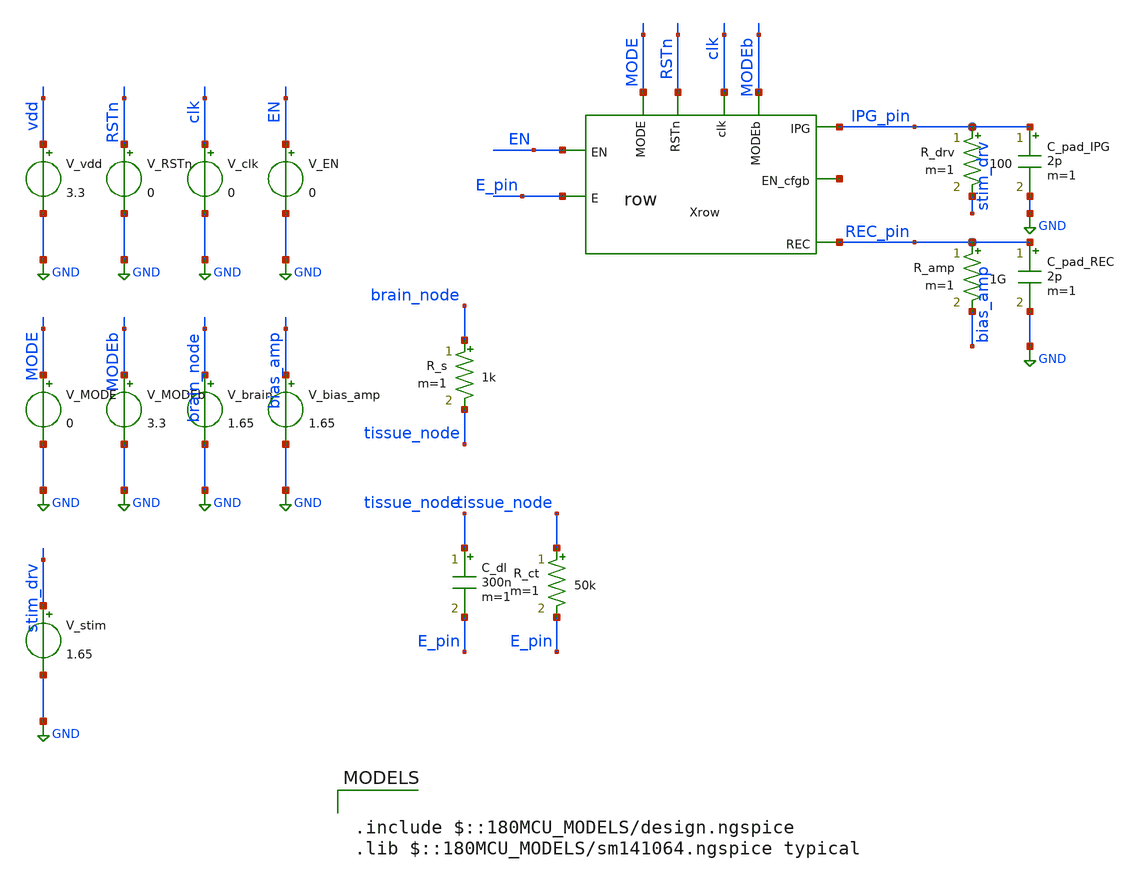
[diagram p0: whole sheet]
** sch_path: tb_realistic.sch
**.subckt tb_realistic
V_vdd vdd GND 3.3
V_RSTn RSTn GND 0
V_clk clk GND 0
V_EN EN GND 0
V_MODE MODE GND 0
V_MODEb MODEb GND 3.3
V_brain brain_node GND 1.65
V_bias_amp bias_amp GND 1.65
V_stim stim_drv GND 1.65
Xrow IPG_pin MODEb EN net1 clk E_pin MODE RSTn REC_pin row
R_s brain_node tissue_node 1k m=1
R_ct tissue_node E_pin 50k m=1
C_dl tissue_node E_pin 300n m=1
R_drv IPG_pin stim_drv 100 m=1
C_pad_IPG IPG_pin GND 2p m=1
R_amp REC_pin bias_amp 1G m=1
C_pad_REC REC_pin GND 2p m=1
**** begin user architecture code

.include $::180MCU_MODELS/design.ngspice
.lib $::180MCU_MODELS/sm141064.ngspice typical



.control
save all

** RSTn: low until 100ns then high
alter @V_RSTn[PWL] = [ 0 0  100n 0  100.001n 3.3  30m 3.3 ]

** Single latching clock pulse around 200ns
alter @V_clk[PWL] = [ 0 0  200n 0  200.001n 3.3  300n 3.3  300.001n 0  30m 0 ]

** EN: high after RSTn release
alter @V_EN[PWL] = [ 0 0  150n 0  150.001n 3.3  30m 3.3 ]

** MODE: stim phase 0-15ms (includes drain), record phase 15-30ms
alter @V_MODE[PWL]  = [ 0 0    15m 0    15.0001m 3.3   30m 3.3 ]
alter @V_MODEb[PWL] = [ 0 3.3  15m 3.3  15.0001m 0     30m 0 ]

** Brain LFP: 100uV sine at 1kHz on 1.65V mid-rail
alter @V_brain[SIN] = [ 1.65 10m 1k 0 0 0 ]

** Stim driver: biphasic pulses at 0.5/1.5/2.5/3.5/4.5 ms during stim phase,
** then held at mid-rail for 10 ms drain before MODE switches.
alter @V_stim[PWL] = [  0          1.65  500u       1.65  500.001u   0.65  600u       0.65  600.001u
+   2.65  700u       2.65  700.001u   1.65  1500u      1.65  1500.001u  0.65  1600u      0.65  1600.001u
+  2.65  1700u      2.65  1700.001u  1.65  2500u      1.65  2500.001u  0.65  2600u      0.65  2600.001u
+  2.65  2700u      2.65  2700.001u  1.65  3500u      1.65  3500.001u  0.65  3600u      0.65  3600.001u
+  2.65  3700u      2.65  3700.001u  1.65  4500u      1.65  4500.001u  0.65  4600u      0.65  4600.001u
+  2.65  4700u      2.65  4700.001u  1.65  30m        1.65 ]

tran 1u 30m 0 5u

** plots
set color0 = white
plot (v(MODE)/6.6)+1.4 v(REC_pin) v(E_pin) v(IPG_pin)/3 + (1.65-1.65/3)

write tb_realistic.raw
.endc


**** end user architecture code
**.ends

* expanding   symbol:  row.sym # of pins=9
** sym_path: row.sym
** sch_path: row.sch
.subckt row IPG MODEb EN EN_cfgb clk E MODE RSTn REC
*.ipin EN
*.ipin clk
*.ipin MODEb
*.ipin MODE
*.ipin E
*.opin IPG
*.opin REC
*.ipin RSTn
*.opin EN_cfgb
x1 EN_cfg SW_IPG MODEb AND
x2 vdd RSTn EN EN_cfg EN_cfgb clk GND DFF
x3 IPG SW_IPG SW_IPGb E TGATE
x4 EN_cfg SW_REC MODE AND
x6 REC SW_REC SW_RECb E TGATE
x5 SW_IPGb SW_IPG INV
x7 SW_RECb SW_REC INV
.ends


* expanding   symbol:  AND/AND.sym # of pins=3
** sym_path: AND/AND.sym
** sch_path: AND/AND.sch
.subckt AND IN0 OUT IN1
*.opin OUT
*.ipin IN0
*.ipin IN1
XM1 net1 IN0 net2 GND nfet_03v3 L=0.28u W=1u nf=1 ad='int((nf+1)/2) * W/nf * 0.18u' as='int((nf+2)/2) * W/nf * 0.18u'
+ pd='2*int((nf+1)/2) * (W/nf + 0.18u)' ps='2*int((nf+2)/2) * (W/nf + 0.18u)' nrd='0.18u / W' nrs='0.18u / W'
+ sa=0 sb=0 sd=0 m=1
XM2 net2 IN1 GND GND nfet_03v3 L=0.28u W=1u nf=1 ad='int((nf+1)/2) * W/nf * 0.18u' as='int((nf+2)/2) * W/nf * 0.18u'
+ pd='2*int((nf+1)/2) * (W/nf + 0.18u)' ps='2*int((nf+2)/2) * (W/nf + 0.18u)' nrd='0.18u / W' nrs='0.18u / W'
+ sa=0 sb=0 sd=0 m=1
XM3 net1 IN0 vdd vdd pfet_03v3 L=0.28u W=1u nf=1 ad='int((nf+1)/2) * W/nf * 0.18u' as='int((nf+2)/2) * W/nf * 0.18u'
+ pd='2*int((nf+1)/2) * (W/nf + 0.18u)' ps='2*int((nf+2)/2) * (W/nf + 0.18u)' nrd='0.18u / W' nrs='0.18u / W'
+ sa=0 sb=0 sd=0 m=1
XM4 net1 IN1 vdd vdd pfet_03v3 L=0.28u W=1u nf=1 ad='int((nf+1)/2) * W/nf * 0.18u' as='int((nf+2)/2) * W/nf * 0.18u'
+ pd='2*int((nf+1)/2) * (W/nf + 0.18u)' ps='2*int((nf+2)/2) * (W/nf + 0.18u)' nrd='0.18u / W' nrs='0.18u / W'
+ sa=0 sb=0 sd=0 m=1
x1 OUT net1 INV
.ends


* expanding   symbol:  DFF/DFF.sym # of pins=7
** sym_path: DFF/DFF.sym
** sch_path: DFF/DFF.sch
.subckt DFF vdd RSTn D Q Qb CLK vss
*.ipin D
*.ipin CLK
*.ipin RSTn
*.opin Q
*.iopin vdd
*.iopin vss
*.opin Qb
XM1 net1 D net3 vss nfet_03v3 L=0.28u W=1u nf=1 ad='int((nf+1)/2) * W/nf * 0.18u' as='int((nf+2)/2) * W/nf * 0.18u'
+ pd='2*int((nf+1)/2) * (W/nf + 0.18u)' ps='2*int((nf+2)/2) * (W/nf + 0.18u)' nrd='0.18u / W' nrs='0.18u / W'
+ sa=0 sb=0 sd=0 m=1
XM2 net1 D net2 vdd pfet_03v3 L=0.28u W=1u nf=1 ad='int((nf+1)/2) * W/nf * 0.18u' as='int((nf+2)/2) * W/nf * 0.18u'
+ pd='2*int((nf+1)/2) * (W/nf + 0.18u)' ps='2*int((nf+2)/2) * (W/nf + 0.18u)' nrd='0.18u / W' nrs='0.18u / W'
+ sa=0 sb=0 sd=0 m=1
XM3 net2 c vdd vdd pfet_03v3 L=0.28u W=1u nf=1 ad='int((nf+1)/2) * W/nf * 0.18u' as='int((nf+2)/2) * W/nf * 0.18u'
+ pd='2*int((nf+1)/2) * (W/nf + 0.18u)' ps='2*int((nf+2)/2) * (W/nf + 0.18u)' nrd='0.18u / W' nrs='0.18u / W'
+ sa=0 sb=0 sd=0 m=1
XM4 net3 cbar vss vss nfet_03v3 L=0.28u W=1u nf=1 ad='int((nf+1)/2) * W/nf * 0.18u' as='int((nf+2)/2) * W/nf * 0.18u'
+ pd='2*int((nf+1)/2) * (W/nf + 0.18u)' ps='2*int((nf+2)/2) * (W/nf + 0.18u)' nrd='0.18u / W' nrs='0.18u / W'
+ sa=0 sb=0 sd=0 m=1
XM5 cbar CLK vss vss nfet_03v3 L=0.28u W=1u nf=1 ad='int((nf+1)/2) * W/nf * 0.18u' as='int((nf+2)/2) * W/nf * 0.18u'
+ pd='2*int((nf+1)/2) * (W/nf + 0.18u)' ps='2*int((nf+2)/2) * (W/nf + 0.18u)' nrd='0.18u / W' nrs='0.18u / W'
+ sa=0 sb=0 sd=0 m=1
XM6 cbar CLK vdd vdd pfet_03v3 L=0.28u W=1u nf=1 ad='int((nf+1)/2) * W/nf * 0.18u' as='int((nf+2)/2) * W/nf * 0.18u'
+ pd='2*int((nf+1)/2) * (W/nf + 0.18u)' ps='2*int((nf+2)/2) * (W/nf + 0.18u)' nrd='0.18u / W' nrs='0.18u / W'
+ sa=0 sb=0 sd=0 m=1
XM7 c cbar vss vss nfet_03v3 L=0.28u W=1u nf=1 ad='int((nf+1)/2) * W/nf * 0.18u' as='int((nf+2)/2) * W/nf * 0.18u'
+ pd='2*int((nf+1)/2) * (W/nf + 0.18u)' ps='2*int((nf+2)/2) * (W/nf + 0.18u)' nrd='0.18u / W' nrs='0.18u / W'
+ sa=0 sb=0 sd=0 m=1
XM8 c cbar vdd vdd pfet_03v3 L=0.28u W=1u nf=1 ad='int((nf+1)/2) * W/nf * 0.18u' as='int((nf+2)/2) * W/nf * 0.18u'
+ pd='2*int((nf+1)/2) * (W/nf + 0.18u)' ps='2*int((nf+2)/2) * (W/nf + 0.18u)' nrd='0.18u / W' nrs='0.18u / W'
+ sa=0 sb=0 sd=0 m=1
XM11 net5 RSTn net4 vss nfet_03v3 L=0.28u W=1u nf=1 ad='int((nf+1)/2) * W/nf * 0.18u' as='int((nf+2)/2) * W/nf * 0.18u'
+ pd='2*int((nf+1)/2) * (W/nf + 0.18u)' ps='2*int((nf+2)/2) * (W/nf + 0.18u)' nrd='0.18u / W' nrs='0.18u / W'
+ sa=0 sb=0 sd=0 m=1
XM12 net4 net6 vss vss nfet_03v3 L=0.28u W=1u nf=1 ad='int((nf+1)/2) * W/nf * 0.18u' as='int((nf+2)/2) * W/nf * 0.18u'
+ pd='2*int((nf+1)/2) * (W/nf + 0.18u)' ps='2*int((nf+2)/2) * (W/nf + 0.18u)' nrd='0.18u / W' nrs='0.18u / W'
+ sa=0 sb=0 sd=0 m=1
XM13 net5 RSTn vdd vdd pfet_03v3 L=0.28u W=1u nf=1 ad='int((nf+1)/2) * W/nf * 0.18u' as='int((nf+2)/2) * W/nf * 0.18u'
+ pd='2*int((nf+1)/2) * (W/nf + 0.18u)' ps='2*int((nf+2)/2) * (W/nf + 0.18u)' nrd='0.18u / W' nrs='0.18u / W'
+ sa=0 sb=0 sd=0 m=1
XM14 net5 net6 vdd vdd pfet_03v3 L=0.28u W=1u nf=1 ad='int((nf+1)/2) * W/nf * 0.18u' as='int((nf+2)/2) * W/nf * 0.18u'
+ pd='2*int((nf+1)/2) * (W/nf + 0.18u)' ps='2*int((nf+2)/2) * (W/nf + 0.18u)' nrd='0.18u / W' nrs='0.18u / W'
+ sa=0 sb=0 sd=0 m=1
XM15 net6 net1 vss vss nfet_03v3 L=0.28u W=1u nf=1 ad='int((nf+1)/2) * W/nf * 0.18u' as='int((nf+2)/2) * W/nf * 0.18u'
+ pd='2*int((nf+1)/2) * (W/nf + 0.18u)' ps='2*int((nf+2)/2) * (W/nf + 0.18u)' nrd='0.18u / W' nrs='0.18u / W'
+ sa=0 sb=0 sd=0 m=1
XM16 net6 net1 vdd vdd pfet_03v3 L=0.28u W=1u nf=1 ad='int((nf+1)/2) * W/nf * 0.18u' as='int((nf+2)/2) * W/nf * 0.18u'
+ pd='2*int((nf+1)/2) * (W/nf + 0.18u)' ps='2*int((nf+2)/2) * (W/nf + 0.18u)' nrd='0.18u / W' nrs='0.18u / W'
+ sa=0 sb=0 sd=0 m=1
XM21 net9 net7 net8 vss nfet_03v3 L=0.28u W=1u nf=1 ad='int((nf+1)/2) * W/nf * 0.18u' as='int((nf+2)/2) * W/nf * 0.18u'
+ pd='2*int((nf+1)/2) * (W/nf + 0.18u)' ps='2*int((nf+2)/2) * (W/nf + 0.18u)' nrd='0.18u / W' nrs='0.18u / W'
+ sa=0 sb=0 sd=0 m=1
XM22 net8 RSTn vss vss nfet_03v3 L=0.28u W=1u nf=1 ad='int((nf+1)/2) * W/nf * 0.18u' as='int((nf+2)/2) * W/nf * 0.18u'
+ pd='2*int((nf+1)/2) * (W/nf + 0.18u)' ps='2*int((nf+2)/2) * (W/nf + 0.18u)' nrd='0.18u / W' nrs='0.18u / W'
+ sa=0 sb=0 sd=0 m=1
XM23 net9 net7 vdd vdd pfet_03v3 L=0.28u W=1u nf=1 ad='int((nf+1)/2) * W/nf * 0.18u' as='int((nf+2)/2) * W/nf * 0.18u'
+ pd='2*int((nf+1)/2) * (W/nf + 0.18u)' ps='2*int((nf+2)/2) * (W/nf + 0.18u)' nrd='0.18u / W' nrs='0.18u / W'
+ sa=0 sb=0 sd=0 m=1
XM24 net9 RSTn vdd vdd pfet_03v3 L=0.28u W=1u nf=1 ad='int((nf+1)/2) * W/nf * 0.18u' as='int((nf+2)/2) * W/nf * 0.18u'
+ pd='2*int((nf+1)/2) * (W/nf + 0.18u)' ps='2*int((nf+2)/2) * (W/nf + 0.18u)' nrd='0.18u / W' nrs='0.18u / W'
+ sa=0 sb=0 sd=0 m=1
XM25 Q net9 vss vss nfet_03v3 L=0.28u W=1u nf=1 ad='int((nf+1)/2) * W/nf * 0.18u' as='int((nf+2)/2) * W/nf * 0.18u'
+ pd='2*int((nf+1)/2) * (W/nf + 0.18u)' ps='2*int((nf+2)/2) * (W/nf + 0.18u)' nrd='0.18u / W' nrs='0.18u / W'
+ sa=0 sb=0 sd=0 m=1
XM26 Q net9 vdd vdd pfet_03v3 L=0.28u W=1u nf=1 ad='int((nf+1)/2) * W/nf * 0.18u' as='int((nf+2)/2) * W/nf * 0.18u'
+ pd='2*int((nf+1)/2) * (W/nf + 0.18u)' ps='2*int((nf+2)/2) * (W/nf + 0.18u)' nrd='0.18u / W' nrs='0.18u / W'
+ sa=0 sb=0 sd=0 m=1
XM19 net7 net9 net11 vss nfet_03v3 L=0.28u W=1u nf=1 ad='int((nf+1)/2) * W/nf * 0.18u' as='int((nf+2)/2) * W/nf * 0.18u'
+ pd='2*int((nf+1)/2) * (W/nf + 0.18u)' ps='2*int((nf+2)/2) * (W/nf + 0.18u)' nrd='0.18u / W' nrs='0.18u / W'
+ sa=0 sb=0 sd=0 m=1
XM20 net7 net9 net10 vdd pfet_03v3 L=0.28u W=1u nf=1 ad='int((nf+1)/2) * W/nf * 0.18u' as='int((nf+2)/2) * W/nf * 0.18u'
+ pd='2*int((nf+1)/2) * (W/nf + 0.18u)' ps='2*int((nf+2)/2) * (W/nf + 0.18u)' nrd='0.18u / W' nrs='0.18u / W'
+ sa=0 sb=0 sd=0 m=1
XM31 net10 c vdd vdd pfet_03v3 L=0.28u W=1u nf=1 ad='int((nf+1)/2) * W/nf * 0.18u' as='int((nf+2)/2) * W/nf * 0.18u'
+ pd='2*int((nf+1)/2) * (W/nf + 0.18u)' ps='2*int((nf+2)/2) * (W/nf + 0.18u)' nrd='0.18u / W' nrs='0.18u / W'
+ sa=0 sb=0 sd=0 m=1
XM32 net11 cbar vss vss nfet_03v3 L=0.28u W=1u nf=1 ad='int((nf+1)/2) * W/nf * 0.18u' as='int((nf+2)/2) * W/nf * 0.18u'
+ pd='2*int((nf+1)/2) * (W/nf + 0.18u)' ps='2*int((nf+2)/2) * (W/nf + 0.18u)' nrd='0.18u / W' nrs='0.18u / W'
+ sa=0 sb=0 sd=0 m=1
XM35 net12 net9 vss vss nfet_03v3 L=0.28u W=1u nf=1 ad='int((nf+1)/2) * W/nf * 0.18u' as='int((nf+2)/2) * W/nf * 0.18u'
+ pd='2*int((nf+1)/2) * (W/nf + 0.18u)' ps='2*int((nf+2)/2) * (W/nf + 0.18u)' nrd='0.18u / W' nrs='0.18u / W'
+ sa=0 sb=0 sd=0 m=1
XM36 net12 net9 vdd vdd pfet_03v3 L=0.28u W=1u nf=1 ad='int((nf+1)/2) * W/nf * 0.18u' as='int((nf+2)/2) * W/nf * 0.18u'
+ pd='2*int((nf+1)/2) * (W/nf + 0.18u)' ps='2*int((nf+2)/2) * (W/nf + 0.18u)' nrd='0.18u / W' nrs='0.18u / W'
+ sa=0 sb=0 sd=0 m=1
XM37 Qb net12 vss vss nfet_03v3 L=0.28u W=1u nf=1 ad='int((nf+1)/2) * W/nf * 0.18u' as='int((nf+2)/2) * W/nf * 0.18u'
+ pd='2*int((nf+1)/2) * (W/nf + 0.18u)' ps='2*int((nf+2)/2) * (W/nf + 0.18u)' nrd='0.18u / W' nrs='0.18u / W'
+ sa=0 sb=0 sd=0 m=1
XM38 Qb net12 vdd vdd pfet_03v3 L=0.28u W=1u nf=1 ad='int((nf+1)/2) * W/nf * 0.18u' as='int((nf+2)/2) * W/nf * 0.18u'
+ pd='2*int((nf+1)/2) * (W/nf + 0.18u)' ps='2*int((nf+2)/2) * (W/nf + 0.18u)' nrd='0.18u / W' nrs='0.18u / W'
+ sa=0 sb=0 sd=0 m=1
XM9 net1 c net5 vss nfet_03v3 L=0.28u W=1u nf=1 ad='int((nf+1)/2) * W/nf * 0.18u' as='int((nf+2)/2) * W/nf * 0.18u'
+ pd='2*int((nf+1)/2) * (W/nf + 0.18u)' ps='2*int((nf+2)/2) * (W/nf + 0.18u)' nrd='0.18u / W' nrs='0.18u / W'
+ sa=0 sb=0 sd=0 m=1
XM10 net1 cbar net5 vdd pfet_03v3 L=0.28u W=1u nf=1 ad='int((nf+1)/2) * W/nf * 0.18u' as='int((nf+2)/2) * W/nf * 0.18u'
+ pd='2*int((nf+1)/2) * (W/nf + 0.18u)' ps='2*int((nf+2)/2) * (W/nf + 0.18u)' nrd='0.18u / W' nrs='0.18u / W'
+ sa=0 sb=0 sd=0 m=1
XM17 net6 c net7 vss nfet_03v3 L=0.28u W=1u nf=1 ad='int((nf+1)/2) * W/nf * 0.18u' as='int((nf+2)/2) * W/nf * 0.18u'
+ pd='2*int((nf+1)/2) * (W/nf + 0.18u)' ps='2*int((nf+2)/2) * (W/nf + 0.18u)' nrd='0.18u / W' nrs='0.18u / W'
+ sa=0 sb=0 sd=0 m=1
XM18 net6 cbar net7 vdd pfet_03v3 L=0.28u W=1u nf=1 ad='int((nf+1)/2) * W/nf * 0.18u' as='int((nf+2)/2) * W/nf * 0.18u'
+ pd='2*int((nf+1)/2) * (W/nf + 0.18u)' ps='2*int((nf+2)/2) * (W/nf + 0.18u)' nrd='0.18u / W' nrs='0.18u / W'
+ sa=0 sb=0 sd=0 m=1
.ends


* expanding   symbol:  TGATE/TGATE.sym # of pins=4
** sym_path: TGATE/TGATE.sym
** sch_path: TGATE/TGATE.sch
.subckt TGATE out c cbar in
*.ipin in
*.opin out
*.ipin cbar
*.ipin c
XM1 out cbar in VDD pfet_03v3 L=0.28u W=1u nf=1 ad='int((nf+1)/2) * W/nf * 0.18u' as='int((nf+2)/2) * W/nf * 0.18u'
+ pd='2*int((nf+1)/2) * (W/nf + 0.18u)' ps='2*int((nf+2)/2) * (W/nf + 0.18u)' nrd='0.18u / W' nrs='0.18u / W'
+ sa=0 sb=0 sd=0 m=1
XM2 out c in GND nfet_03v3 L=0.28u W=1u nf=1 ad='int((nf+1)/2) * W/nf * 0.18u' as='int((nf+2)/2) * W/nf * 0.18u'
+ pd='2*int((nf+1)/2) * (W/nf + 0.18u)' ps='2*int((nf+2)/2) * (W/nf + 0.18u)' nrd='0.18u / W' nrs='0.18u / W'
+ sa=0 sb=0 sd=0 m=1
.ends


* expanding   symbol:  AND/INV.sym # of pins=2
** sym_path: AND/INV.sym
** sch_path: AND/INV.sch
.subckt INV OUT IN
*.ipin IN
*.opin OUT
XM1 OUT IN VDD VDD pfet_03v3 L=0.28u W=1u nf=1 ad='int((nf+1)/2) * W/nf * 0.18u' as='int((nf+2)/2) * W/nf * 0.18u'
+ pd='2*int((nf+1)/2) * (W/nf + 0.18u)' ps='2*int((nf+2)/2) * (W/nf + 0.18u)' nrd='0.18u / W' nrs='0.18u / W'
+ sa=0 sb=0 sd=0 m=1
XM2 OUT IN GND GND nfet_03v3 L=0.28u W=0.5u nf=1 ad='int((nf+1)/2) * W/nf * 0.18u' as='int((nf+2)/2) * W/nf * 0.18u'
+ pd='2*int((nf+1)/2) * (W/nf + 0.18u)' ps='2*int((nf+2)/2) * (W/nf + 0.18u)' nrd='0.18u / W' nrs='0.18u / W'
+ sa=0 sb=0 sd=0 m=1
.ends

.GLOBAL GND
.GLOBAL vdd
.GLOBAL VDD
.end
